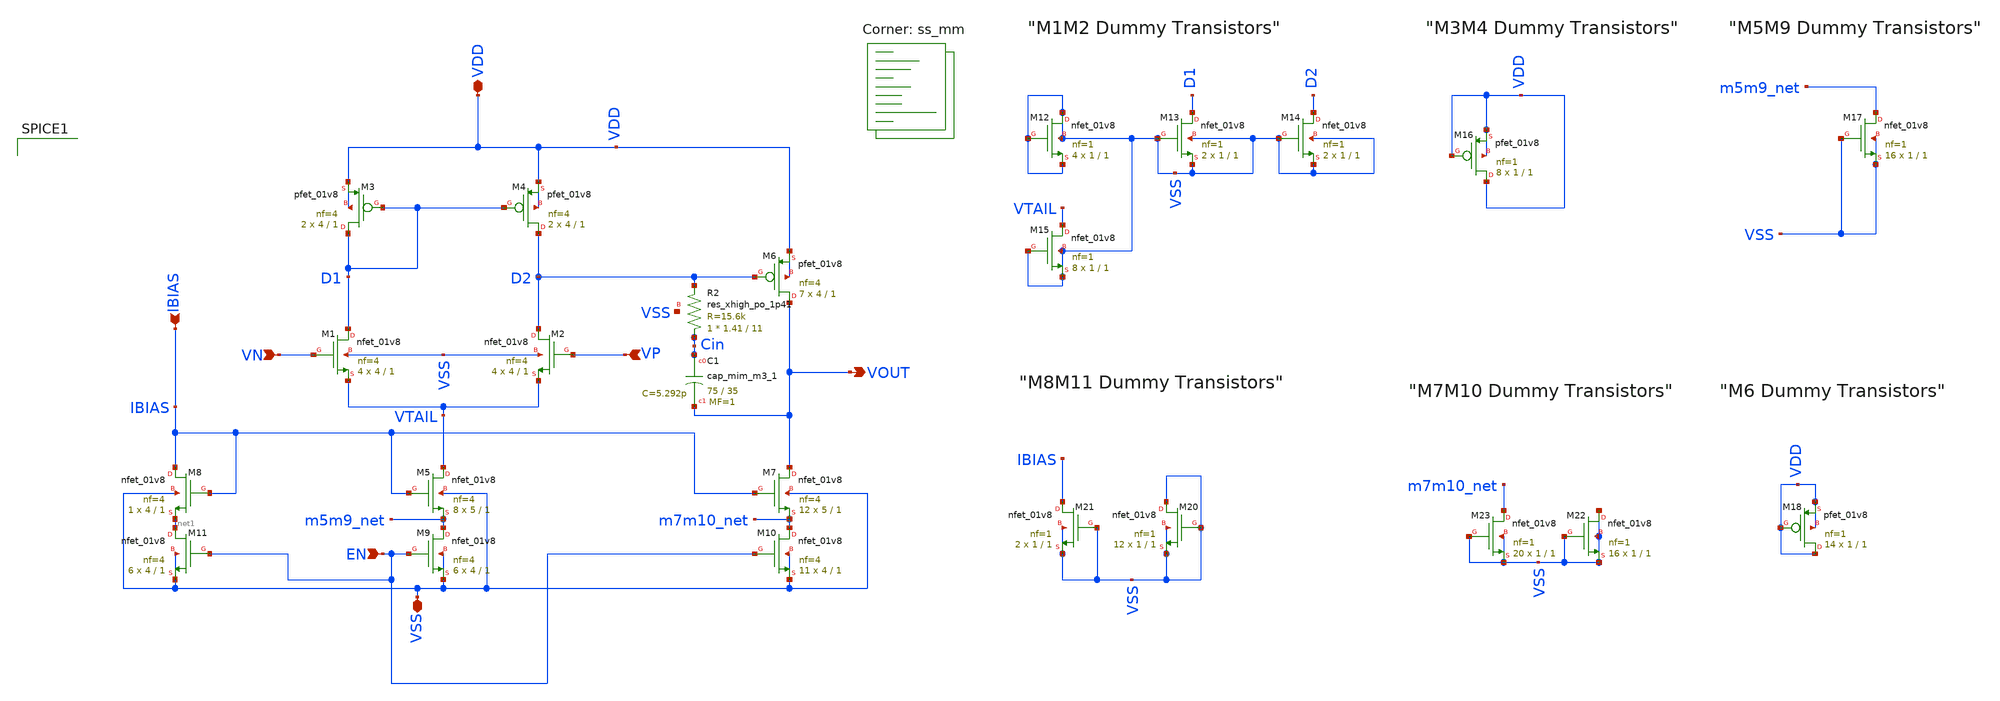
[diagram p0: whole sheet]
** sch_path: xschem/sky130_op_amp.sch
**.subckt sky130_op_amp VN VOUT VDD VSS VP EN IBIAS
*.ipin VN
*.opin VOUT
*.iopin VDD
*.iopin VSS
*.ipin VP
*.ipin EN
*.ipin IBIAS
XM1 D1 VN VTAIL VSS sky130_fd_pr__nfet_01v8 L=1 W=4 nf=4 ad='int((nf+1)/2) * W/nf * 0.29' as='int((nf+2)/2) * W/nf * 0.29'
+ pd='2*int((nf+1)/2) * (W/nf + 0.29)' ps='2*int((nf+2)/2) * (W/nf + 0.29)' nrd='0.29 / W' nrs='0.29 / W'
+ sa=0 sb=0 sd=0 mult=4 m=4
XM2 D2 VP VTAIL VSS sky130_fd_pr__nfet_01v8 L=1 W=4 nf=4 ad='int((nf+1)/2) * W/nf * 0.29' as='int((nf+2)/2) * W/nf * 0.29'
+ pd='2*int((nf+1)/2) * (W/nf + 0.29)' ps='2*int((nf+2)/2) * (W/nf + 0.29)' nrd='0.29 / W' nrs='0.29 / W'
+ sa=0 sb=0 sd=0 mult=4 m=4
XM5 VTAIL IBIAS m5m9_net VSS sky130_fd_pr__nfet_01v8 L=1 W=5 nf=4 ad='int((nf+1)/2) * W/nf * 0.29' as='int((nf+2)/2) * W/nf * 0.29'
+ pd='2*int((nf+1)/2) * (W/nf + 0.29)' ps='2*int((nf+2)/2) * (W/nf + 0.29)' nrd='0.29 / W' nrs='0.29 / W'
+ sa=0 sb=0 sd=0 mult=8 m=8
XM8 IBIAS IBIAS net1 VSS sky130_fd_pr__nfet_01v8 L=1 W=4 nf=4 ad='int((nf+1)/2) * W/nf * 0.29' as='int((nf+2)/2) * W/nf * 0.29'
+ pd='2*int((nf+1)/2) * (W/nf + 0.29)' ps='2*int((nf+2)/2) * (W/nf + 0.29)' nrd='0.29 / W' nrs='0.29 / W'
+ sa=0 sb=0 sd=0 mult=1 m=1
XM3 D1 D1 VDD VDD sky130_fd_pr__pfet_01v8 L=1 W=4 nf=4 ad='int((nf+1)/2) * W/nf * 0.29' as='int((nf+2)/2) * W/nf * 0.29'
+ pd='2*int((nf+1)/2) * (W/nf + 0.29)' ps='2*int((nf+2)/2) * (W/nf + 0.29)' nrd='0.29 / W' nrs='0.29 / W'
+ sa=0 sb=0 sd=0 mult=2 m=2
XM4 D2 D1 VDD VDD sky130_fd_pr__pfet_01v8 L=1 W=4 nf=4 ad='int((nf+1)/2) * W/nf * 0.29' as='int((nf+2)/2) * W/nf * 0.29'
+ pd='2*int((nf+1)/2) * (W/nf + 0.29)' ps='2*int((nf+2)/2) * (W/nf + 0.29)' nrd='0.29 / W' nrs='0.29 / W'
+ sa=0 sb=0 sd=0 mult=2 m=2
XM6 VOUT D2 VDD VDD sky130_fd_pr__pfet_01v8 L=1 W=4 nf=4 ad='int((nf+1)/2) * W/nf * 0.29' as='int((nf+2)/2) * W/nf * 0.29'
+ pd='2*int((nf+1)/2) * (W/nf + 0.29)' ps='2*int((nf+2)/2) * (W/nf + 0.29)' nrd='0.29 / W' nrs='0.29 / W'
+ sa=0 sb=0 sd=0 mult=7 m=7
XM7 VOUT IBIAS m7m10_net VSS sky130_fd_pr__nfet_01v8 L=1 W=5 nf=4 ad='int((nf+1)/2) * W/nf * 0.29' as='int((nf+2)/2) * W/nf * 0.29'
+ pd='2*int((nf+1)/2) * (W/nf + 0.29)' ps='2*int((nf+2)/2) * (W/nf + 0.29)' nrd='0.29 / W' nrs='0.29 / W'
+ sa=0 sb=0 sd=0 mult=12 m=12
XC1 Cin VOUT sky130_fd_pr__cap_mim_m3_1 W=75 L=35 MF=1 m=1
XM9 m5m9_net EN VSS VSS sky130_fd_pr__nfet_01v8 L=1 W=4 nf=4 ad='int((nf+1)/2) * W/nf * 0.29' as='int((nf+2)/2) * W/nf * 0.29'
+ pd='2*int((nf+1)/2) * (W/nf + 0.29)' ps='2*int((nf+2)/2) * (W/nf + 0.29)' nrd='0.29 / W' nrs='0.29 / W'
+ sa=0 sb=0 sd=0 mult=6 m=6
XM10 m7m10_net EN VSS VSS sky130_fd_pr__nfet_01v8 L=1 W=4 nf=4 ad='int((nf+1)/2) * W/nf * 0.29' as='int((nf+2)/2) * W/nf * 0.29'
+ pd='2*int((nf+1)/2) * (W/nf + 0.29)' ps='2*int((nf+2)/2) * (W/nf + 0.29)' nrd='0.29 / W' nrs='0.29 / W'
+ sa=0 sb=0 sd=0 mult=11 m=11
XM11 net1 EN VSS VSS sky130_fd_pr__nfet_01v8 L=1 W=4 nf=4 ad='int((nf+1)/2) * W/nf * 0.29' as='int((nf+2)/2) * W/nf * 0.29'
+ pd='2*int((nf+1)/2) * (W/nf + 0.29)' ps='2*int((nf+2)/2) * (W/nf + 0.29)' nrd='0.29 / W' nrs='0.29 / W'
+ sa=0 sb=0 sd=0 mult=6 m=6
XR2 Cin D2 VSS sky130_fd_pr__res_xhigh_po_1p41 L=11 mult=1 m=1
XM12 VSS VSS VSS VSS sky130_fd_pr__nfet_01v8 L=1 W=1 nf=1 ad='int((nf+1)/2) * W/nf * 0.29' as='int((nf+2)/2) * W/nf * 0.29'
+ pd='2*int((nf+1)/2) * (W/nf + 0.29)' ps='2*int((nf+2)/2) * (W/nf + 0.29)' nrd='0.29 / W' nrs='0.29 / W'
+ sa=0 sb=0 sd=0 mult=4 m=4
XM13 D1 VSS VSS VSS sky130_fd_pr__nfet_01v8 L=1 W=1 nf=1 ad='int((nf+1)/2) * W/nf * 0.29' as='int((nf+2)/2) * W/nf * 0.29'
+ pd='2*int((nf+1)/2) * (W/nf + 0.29)' ps='2*int((nf+2)/2) * (W/nf + 0.29)' nrd='0.29 / W' nrs='0.29 / W'
+ sa=0 sb=0 sd=0 mult=2 m=2
XM14 D2 VSS VSS VSS sky130_fd_pr__nfet_01v8 L=1 W=1 nf=1 ad='int((nf+1)/2) * W/nf * 0.29' as='int((nf+2)/2) * W/nf * 0.29'
+ pd='2*int((nf+1)/2) * (W/nf + 0.29)' ps='2*int((nf+2)/2) * (W/nf + 0.29)' nrd='0.29 / W' nrs='0.29 / W'
+ sa=0 sb=0 sd=0 mult=2 m=2
XM15 VTAIL VSS VSS VSS sky130_fd_pr__nfet_01v8 L=1 W=1 nf=1 ad='int((nf+1)/2) * W/nf * 0.29' as='int((nf+2)/2) * W/nf * 0.29'
+ pd='2*int((nf+1)/2) * (W/nf + 0.29)' ps='2*int((nf+2)/2) * (W/nf + 0.29)' nrd='0.29 / W' nrs='0.29 / W'
+ sa=0 sb=0 sd=0 mult=8 m=8
XM16 VDD VDD VDD VDD sky130_fd_pr__pfet_01v8 L=1 W=1 nf=1 ad='int((nf+1)/2) * W/nf * 0.29' as='int((nf+2)/2) * W/nf * 0.29'
+ pd='2*int((nf+1)/2) * (W/nf + 0.29)' ps='2*int((nf+2)/2) * (W/nf + 0.29)' nrd='0.29 / W' nrs='0.29 / W'
+ sa=0 sb=0 sd=0 mult=8 m=8
XM17 m5m9_net VSS VSS VSS sky130_fd_pr__nfet_01v8 L=1 W=1 nf=1 ad='int((nf+1)/2) * W/nf * 0.29' as='int((nf+2)/2) * W/nf * 0.29'
+ pd='2*int((nf+1)/2) * (W/nf + 0.29)' ps='2*int((nf+2)/2) * (W/nf + 0.29)' nrd='0.29 / W' nrs='0.29 / W'
+ sa=0 sb=0 sd=0 mult=16 m=16
XM20 VSS VSS VSS VSS sky130_fd_pr__nfet_01v8 L=1 W=1 nf=1 ad='int((nf+1)/2) * W/nf * 0.29' as='int((nf+2)/2) * W/nf * 0.29'
+ pd='2*int((nf+1)/2) * (W/nf + 0.29)' ps='2*int((nf+2)/2) * (W/nf + 0.29)' nrd='0.29 / W' nrs='0.29 / W'
+ sa=0 sb=0 sd=0 mult=12 m=12
XM21 IBIAS VSS VSS VSS sky130_fd_pr__nfet_01v8 L=1 W=1 nf=1 ad='int((nf+1)/2) * W/nf * 0.29' as='int((nf+2)/2) * W/nf * 0.29'
+ pd='2*int((nf+1)/2) * (W/nf + 0.29)' ps='2*int((nf+2)/2) * (W/nf + 0.29)' nrd='0.29 / W' nrs='0.29 / W'
+ sa=0 sb=0 sd=0 mult=2 m=2
XM22 VSS VSS VSS VSS sky130_fd_pr__nfet_01v8 L=1 W=1 nf=1 ad='int((nf+1)/2) * W/nf * 0.29' as='int((nf+2)/2) * W/nf * 0.29'
+ pd='2*int((nf+1)/2) * (W/nf + 0.29)' ps='2*int((nf+2)/2) * (W/nf + 0.29)' nrd='0.29 / W' nrs='0.29 / W'
+ sa=0 sb=0 sd=0 mult=16 m=16
XM23 m7m10_net VSS VSS VSS sky130_fd_pr__nfet_01v8 L=1 W=1 nf=1 ad='int((nf+1)/2) * W/nf * 0.29' as='int((nf+2)/2) * W/nf * 0.29'
+ pd='2*int((nf+1)/2) * (W/nf + 0.29)' ps='2*int((nf+2)/2) * (W/nf + 0.29)' nrd='0.29 / W' nrs='0.29 / W'
+ sa=0 sb=0 sd=0 mult=20 m=20
XM18 VDD VDD VDD VDD sky130_fd_pr__pfet_01v8 L=1 W=1 nf=1 ad='int((nf+1)/2) * W/nf * 0.29' as='int((nf+2)/2) * W/nf * 0.29'
+ pd='2*int((nf+1)/2) * (W/nf + 0.29)' ps='2*int((nf+2)/2) * (W/nf + 0.29)' nrd='0.29 / W' nrs='0.29 / W'
+ sa=0 sb=0 sd=0 mult=14 m=14
**** begin user architecture code
.lib $::SKYWATER_MODELS/sky130.lib.spice ss_mm




**** end user architecture code
**.ends
.end
